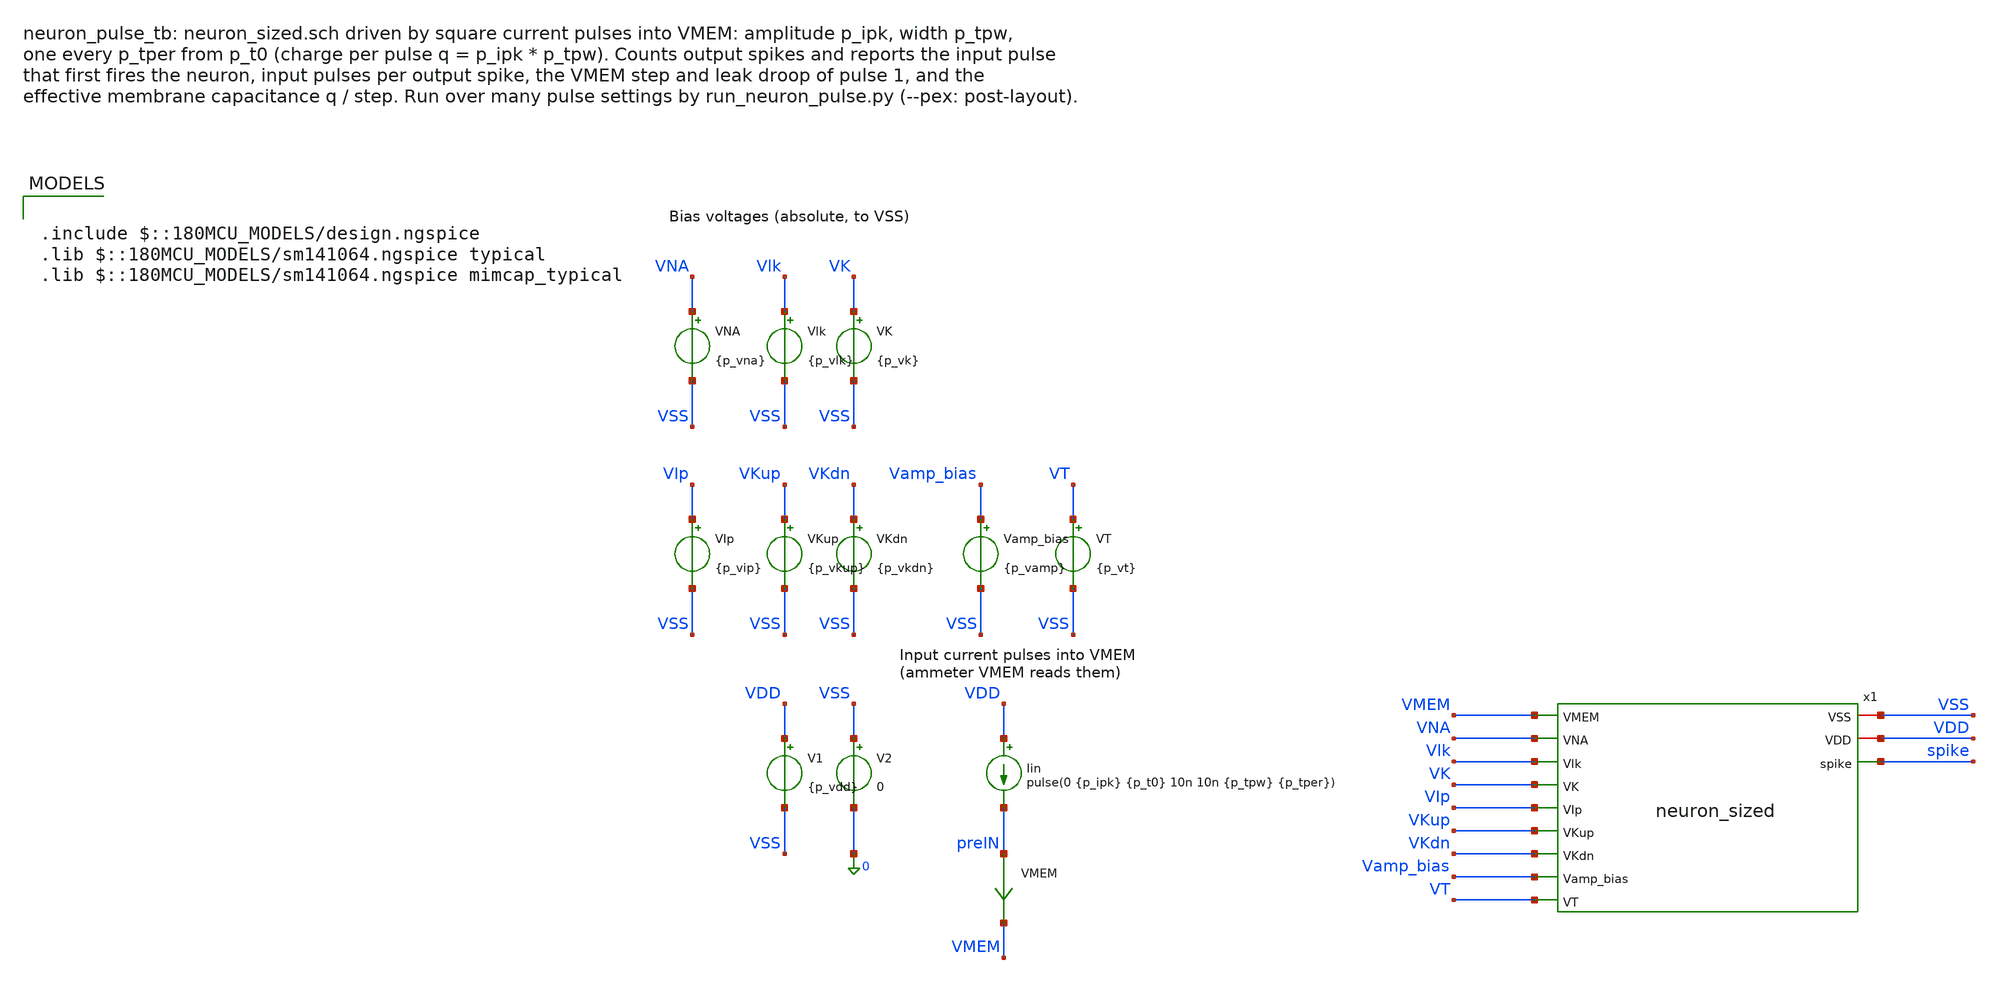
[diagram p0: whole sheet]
** sch_path: analog/testbenches/neuron/neuron_pulse_tb.sch
**.subckt neuron_pulse_tb
V1 VDD VSS {p_vdd}
V2 VSS 0 0
Iin VDD preIN pulse(0 {p_ipk} {p_t0} 10n 10n {p_tpw} {p_tper})
VMEM preIN VMEM 0
.save i(vmem)
x1 VSS VDD VMEM VNA Vlk VK VIp VKup VKdn Vamp_bias VT spike neuron_sized
Vlk Vlk VSS {p_vlk}
VK VK VSS {p_vk}
VNA VNA VSS {p_vna}
VKup VKup VSS {p_vkup}
VKdn VKdn VSS {p_vkdn}
VIp VIp VSS {p_vip}
VT VT VSS {p_vt}
Vamp_bias Vamp_bias VSS {p_vamp}
**** begin user architecture code

.include $::180MCU_MODELS/design.ngspice
.lib $::180MCU_MODELS/sm141064.ngspice typical
.lib $::180MCU_MODELS/sm141064.ngspice mimcap_typical



* Biases of neuron_sized (as in neuron_nominal_tb). The pulse settings, p_tstop and
* p_tmax (maximum time step) are set per point by run_neuron_pulse.py.
.param p_vdd=3.3 p_ipk=20n p_tpw=10u p_tper=200u p_t0=50u p_tstop=5m p_tmax=100n
.param p_vlk=0.425 p_vamp=0.535 p_vip=0.573 p_vna=1.93 p_vkup=2.35 p_vk=1.22 p_vkdn=0.588 p_vt=1.66
.csparam vdd_c={p_vdd}
.csparam tstop_c={p_tstop}
.csparam tmax_c={p_tmax}
.csparam ipk_c={p_ipk}
.csparam tpw_c={p_tpw}
.csparam tper_c={p_tper}
.csparam t0_c={p_t0}
.ic v(VMEM)=0 v(spike)=0
.control
  save v(spike) v(VMEM) i(VMEM)
  tran 20n $&tstop_c 0 $&tmax_c uic
  let vsw = vdd_c/2

  * Output spikes: rising edges of spike through VDD/2 (a failed meas keeps -1)
  let n = 0
  let k = 1
  let t1 = -1
  let tlast = -1
  while k <= 2000
    let tk = -1
    meas tran tk when v(spike)=$&vsw rise=$&k
    if tk < 0
      break
    end
    if k = 1
      let t1 = tk
    end
    let tlast = tk
    let n = k
    let k = k + 1
  end

  * Input pulses that started at least 30 us before the end of the run (a later
  * one may not have had time to fire the neuron)
  let n_in = floor((tstop_c - 30u - t0_c)/tper_c) + 1
  * Input pulse during which (or after which) the first output spike came
  let n_first = 0
  if n >= 1
    let n_first = floor((t1 - t0_c)/tper_c) + 1
  end
  * Input pulses per output spike after the first one
  let n_per = 0
  if n >= 2
    let n_per = (tlast - t1)/((n - 1)*tper_c)
  end

  * Pulse 1: charge delivered, VMEM step, leak droop until just before pulse 2
  let q = ipk_c*tpw_c
  let ta = t0_c - 1u
  let tb = t0_c + tpw_c + 0.5u
  let tc = t0_c + tper_c - 0.5u
  meas tran v_a find v(VMEM) at=$&ta
  meas tran v_b find v(VMEM) at=$&tb
  meas tran v_c find v(VMEM) at=$&tc
  meas tran q1 integ i(VMEM) from=$&ta to=$&tb
  let dv1 = v_b - v_a
  let droop1 = v_b - v_c
  let c_eff = 0
  if dv1 > 1m
    let c_eff = q1/dv1
  end

  echo RES ipk=$&ipk_c
  echo RES tpw=$&tpw_c
  echo RES tper=$&tper_c
  echo RES q=$&q
  echo RES q1=$&q1
  echo RES n_in=$&n_in
  echo RES nspikes=$&n
  echo RES n_first=$&n_first
  echo RES n_per=$&n_per
  echo RES t_first=$&t1
  echo RES dv1=$&dv1
  echo RES droop1=$&droop1
  echo RES c_eff=$&c_eff
  echo neuron_pulse_tb: q $&q C per pulse, $&n output spikes for $&n_in input pulses, first after
+ pulse $&n_first, then one per $&n_per pulses

  set wr_singlescale
  set wr_vecnames
  if $?batchmode = 0
    wrdata /foss/designs/engn2912e-project/analog/testbenches/neuron/results/neuron_pulse_tb.txt
+ v(VMEM) v(spike) i(VMEM)
    plot v(VMEM) v(spike) title 'neuron_pulse_tb: membrane and spike' xlabel 't (s)' ylabel 'V'
    plot i(VMEM) title 'neuron_pulse_tb: input current' xlabel 't (s)' ylabel 'A'
  else
    wrdata neuron_pulse_tb.txt v(VMEM) v(spike) i(VMEM)
  end
.endc


**** end user architecture code
**.ends
.end
